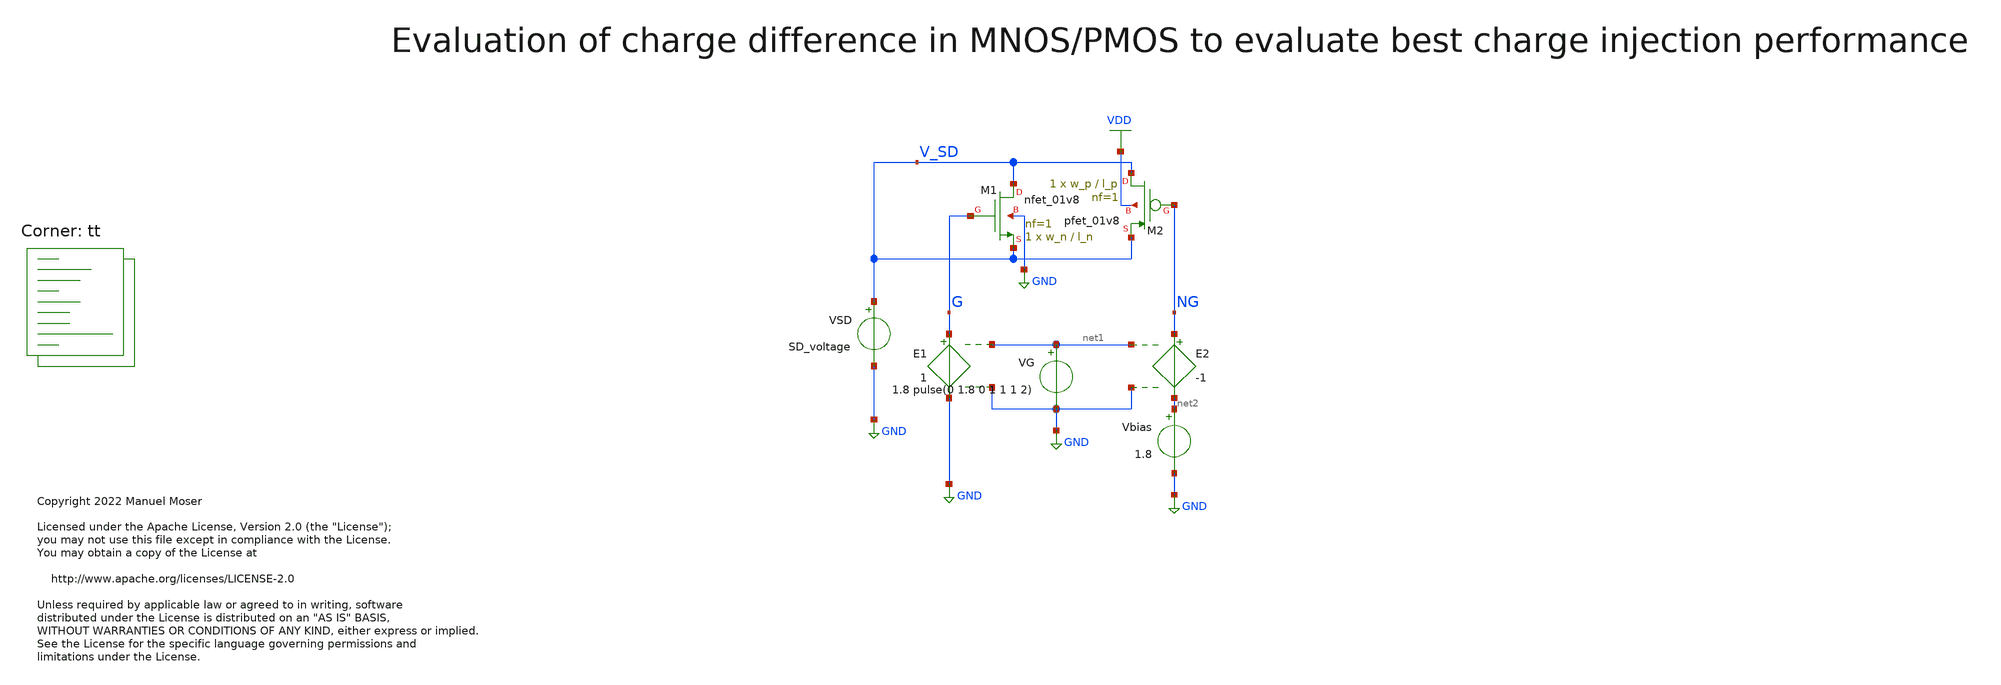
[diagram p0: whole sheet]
** sch_path: xschem/archive/adc_vcm_switch_tb_charge.sch
* Copyright 2022 Manuel Moser
* Licensed under the Apache License, Version 2.0 (the "License");
**.subckt adc_vcm_switch_tb_charge
VSD V_SD GND SD_voltage
XM1 V_SD G V_SD GND sky130_fd_pr__nfet_01v8 L=l_n W=w_n nf=1 ad='int((nf+1)/2) * W/nf * 0.29' as='int((nf+2)/2) * W/nf * 0.29'
+ pd='2*int((nf+1)/2) * (W/nf + 0.29)' ps='2*int((nf+2)/2) * (W/nf + 0.29)' nrd='0.29 / W' nrs='0.29 / W'
+ sa=0 sb=0 sd=0 mult=1 m=1
XM2 V_SD NG V_SD VDD sky130_fd_pr__pfet_01v8 L=l_p W=w_p nf=1 ad='int((nf+1)/2) * W/nf * 0.29' as='int((nf+2)/2) * W/nf * 0.29'
+ pd='2*int((nf+1)/2) * (W/nf + 0.29)' ps='2*int((nf+2)/2) * (W/nf + 0.29)' nrd='0.29 / W' nrs='0.29 / W'
+ sa=0 sb=0 sd=0 mult=1 m=1
VG net1 GND 1.8 pulse(0 1.8 0 1 1 1 2)
E1 G GND net1 GND 1
E2 NG net2 net1 GND -1
Vbias net2 GND 1.8
**** begin user architecture code
.lib $::SKYWATER_MODELS/sky130.lib.spice tt


.save all
.OPTIONS savecurrents
.OPTIONS RELTOL=.001 TRTOL=1 ABSTOL=1e-16 CHGTOL=1.0e-16 DEFAD=1.0e-16
.save @m.xM1.msky130_fd_pr__nfet_01v8[qg]
.save @m.xM1.msky130_fd_pr__nfet_01v8[qb]
.save @m.xM1.msky130_fd_pr__nfet_01v8[qd]
.save @m.xM1.msky130_fd_pr__nfet_01v8[qs]
.save @m.xM2.msky130_fd_pr__pfet_01v8[qg]
.save @m.xM2.msky130_fd_pr__pfet_01v8[qb]
.save @m.xM2.msky130_fd_pr__pfet_01v8[qd]
.save @m.xM2.msky130_fd_pr__pfet_01v8[qs]

.param w_p=2 l_p = 1
.param w_n=1 l_n=0.5
.param sd_voltage = 0

.ic v(G)=0 v(GN)=1.8

.control
alterparam w_p=2 l_p = 1
alterparam w_n=1 l_n=0.5
alterparam SD_voltage=0
reset
tran 1m 1
write tran.out @m.xM1.msky130_fd_pr__nfet_01v8[qg] @m.xM1.msky130_fd_pr__nfet_01v8[qd]
+ @m.xM1.msky130_fd_pr__nfet_01v8[qs] @m.xM2.msky130_fd_pr__pfet_01v8[qg] @m.xM2.msky130_fd_pr__pfet_01v8[qd]
+ @m.xM2.msky130_fd_pr__pfet_01v8[qs]
set appendwrite

alterparam w_p=1 l_p = 0.5
alterparam w_n=1 l_n=0.5
alterparam SD_voltage=0
reset
tran 1m 1
write tran.out @m.xM1.msky130_fd_pr__nfet_01v8[qg] @m.xM1.msky130_fd_pr__nfet_01v8[qd]
+ @m.xM1.msky130_fd_pr__nfet_01v8[qs] @m.xM2.msky130_fd_pr__pfet_01v8[qg] @m.xM2.msky130_fd_pr__pfet_01v8[qd]
+ @m.xM2.msky130_fd_pr__pfet_01v8[qs]
set appendwrite

alterparam w_p=0.42 l_p = 0.15
alterparam w_n=0.42 l_n=0.15
alterparam SD_voltage=0
reset
tran 1m 1
write tran.out @m.xM1.msky130_fd_pr__nfet_01v8[qg] @m.xM1.msky130_fd_pr__nfet_01v8[qd]
+ @m.xM1.msky130_fd_pr__nfet_01v8[qs] @m.xM2.msky130_fd_pr__pfet_01v8[qg] @m.xM2.msky130_fd_pr__pfet_01v8[qd]
+ @m.xM2.msky130_fd_pr__pfet_01v8[qs]
set appendwrite

alterparam w_p=2 l_p = 1
alterparam w_n=1 l_n=0.5
alterparam SD_voltage=1.8
reset
tran 1m 1
write tran.out @m.xM1.msky130_fd_pr__nfet_01v8[qg] @m.xM1.msky130_fd_pr__nfet_01v8[qd]
+ @m.xM1.msky130_fd_pr__nfet_01v8[qs] @m.xM2.msky130_fd_pr__pfet_01v8[qg] @m.xM2.msky130_fd_pr__pfet_01v8[qd]
+ @m.xM2.msky130_fd_pr__pfet_01v8[qs]
set appendwrite

alterparam w_p=1 l_p = 0.5
alterparam w_n=1 l_n=0.5
alterparam SD_voltage=1.8
reset
tran 1m 1
write tran.out @m.xM1.msky130_fd_pr__nfet_01v8[qg] @m.xM1.msky130_fd_pr__nfet_01v8[qd]
+ @m.xM1.msky130_fd_pr__nfet_01v8[qs] @m.xM2.msky130_fd_pr__pfet_01v8[qg] @m.xM2.msky130_fd_pr__pfet_01v8[qd]
+ @m.xM2.msky130_fd_pr__pfet_01v8[qs]
set appendwrite

alterparam w_p=0.42 l_p = 0.15
alterparam w_n=0.42 l_n=0.15
alterparam SD_voltage=1.8
reset
tran 1m 1
write tran.out @m.xM1.msky130_fd_pr__nfet_01v8[qg] @m.xM1.msky130_fd_pr__nfet_01v8[qd]
+ @m.xM1.msky130_fd_pr__nfet_01v8[qs] @m.xM2.msky130_fd_pr__pfet_01v8[qg] @m.xM2.msky130_fd_pr__pfet_01v8[qd]
+ @m.xM2.msky130_fd_pr__pfet_01v8[qs]
set appendwrite

* Charge on NMOS Gate
plot tran1.@m.xM1.msky130_fd_pr__nfet_01v8[qg] tran2.@m.xM1.msky130_fd_pr__nfet_01v8[qg]
+ tran3.@m.xM1.msky130_fd_pr__nfet_01v8[qg] tran4.@m.xM1.msky130_fd_pr__nfet_01v8[qg] tran5.@m.xM1.msky130_fd_pr__nfet_01v8[qg]
+ tran6.@m.xM1.msky130_fd_pr__nfet_01v8[qg]

* Charge on PMOS Gate
plot (-tran1.@m.xM2.msky130_fd_pr__pfet_01v8[qg]) (-tran2.@m.xM2.msky130_fd_pr__pfet_01v8[qg])
+ (-tran3.@m.xM2.msky130_fd_pr__pfet_01v8[qg]) (-tran4.@m.xM2.msky130_fd_pr__pfet_01v8[qg]) (-tran5.@m.xM2.msky130_fd_pr__pfet_01v8[qg])
+ (-tran6.@m.xM2.msky130_fd_pr__pfet_01v8[qg])

* Charge sum on Gates
plot (tran1.@m.xM1.msky130_fd_pr__nfet_01v8[qg]+(-tran1.@m.xM2.msky130_fd_pr__pfet_01v8[qg]))
+ (tran2.@m.xM1.msky130_fd_pr__nfet_01v8[qg]+(-tran2.@m.xM2.msky130_fd_pr__pfet_01v8[qg])) (tran3.@m.xM1.msky130_fd_pr__nfet_01v8[qg]+(-tran3.@m.xM2.msky130_fd_pr__pfet_01v8[qg]))
plot (tran4.@m.xM1.msky130_fd_pr__nfet_01v8[qg]+(-tran4.@m.xM2.msky130_fd_pr__pfet_01v8[qg]))
+  (tran5.@m.xM1.msky130_fd_pr__nfet_01v8[qg]+(-tran5.@m.xM2.msky130_fd_pr__pfet_01v8[qg])) (tran6.@m.xM1.msky130_fd_pr__nfet_01v8[qg]+(-tran6.@m.xM2.msky130_fd_pr__pfet_01v8[qg]))

*plot dc1.@m.xM1.msky130_fd_pr__nfet_01v8[qs] dc2.@m.xM1.msky130_fd_pr__nfet_01v8[qs]
*+ dc3.@m.xM1.msky130_fd_pr__nfet_01v8[qs]
*plot dc1.@m.xM2.msky130_fd_pr__pfet_01v8[qs] dc2.@m.xM2.msky130_fd_pr__pfet_01v8[qs]
*+ dc3.@m.xM2.msky130_fd_pr__pfet_01v8[qs]
.endc


**** end user architecture code
**.ends
.GLOBAL GND
.GLOBAL VDD
.end
